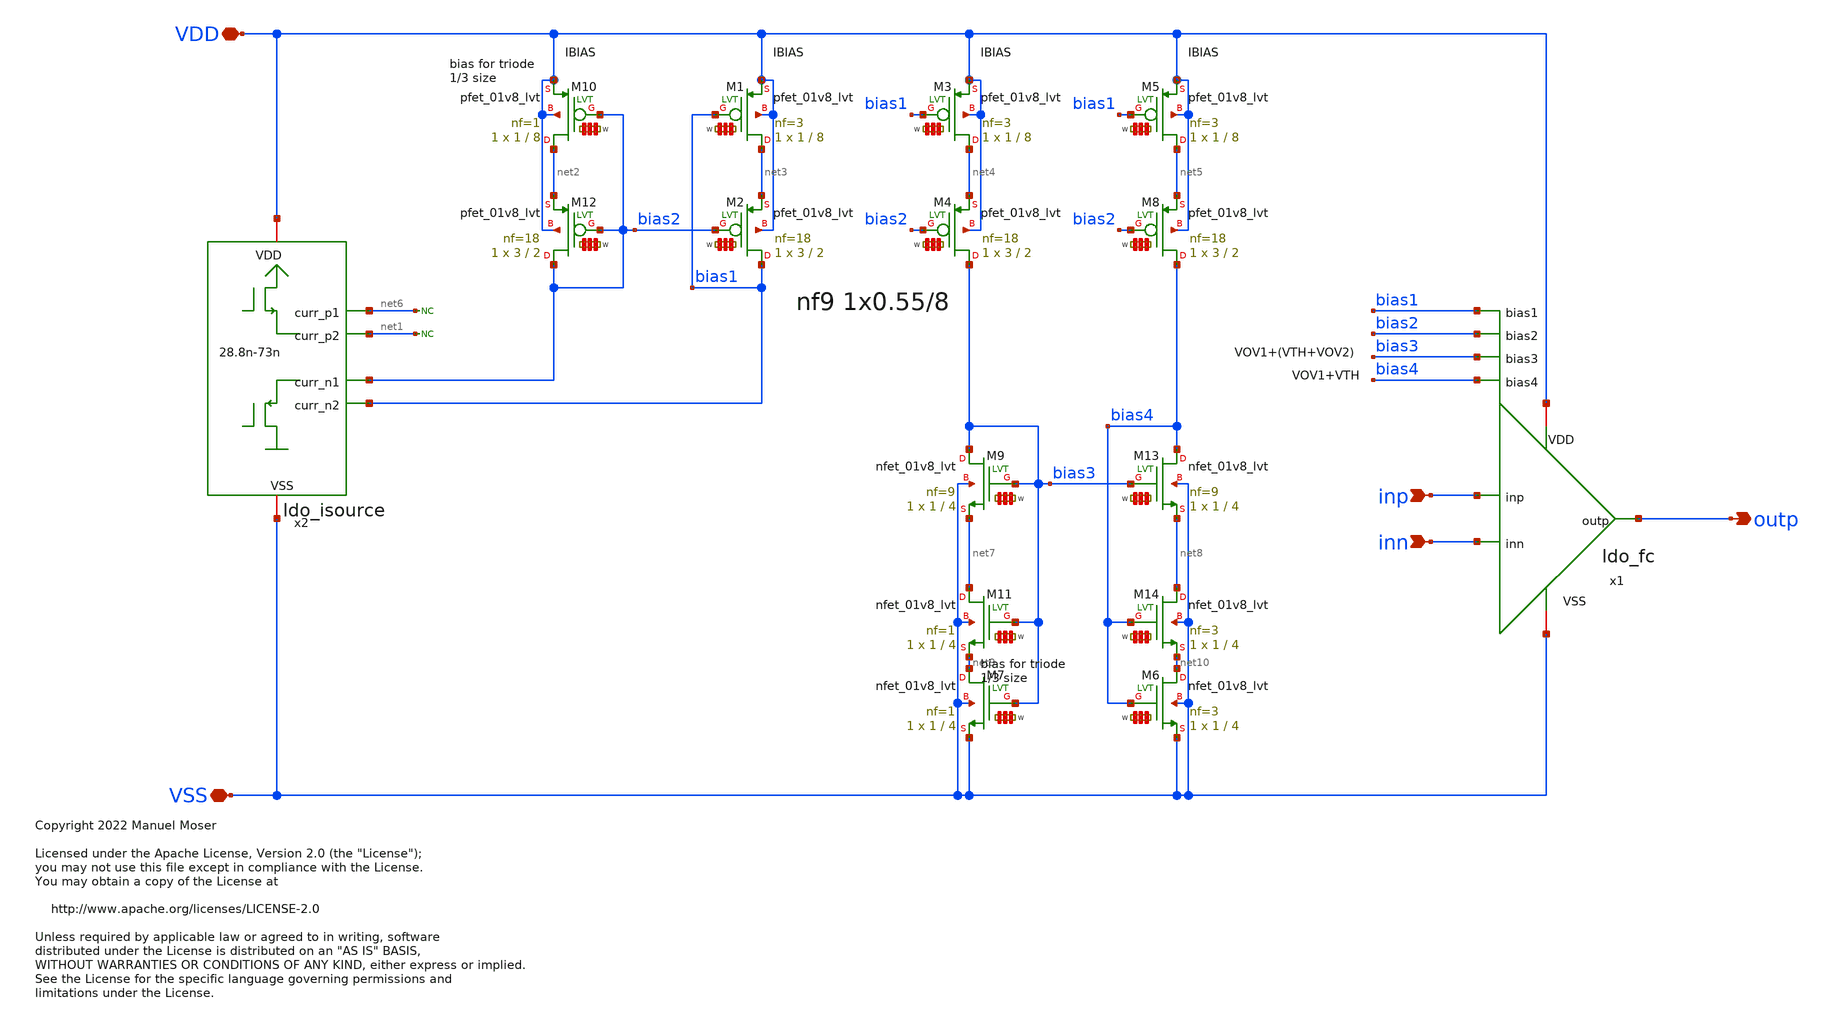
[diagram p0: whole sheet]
** sch_path: xschem/ldo_ota.sch
* Copyright 2022 Manuel Moser
* Licensed under the Apache License, Version 2.0 (the "License");
**.subckt ldo_ota VDD VSS inp inn outp
*.iopin VDD
*.iopin VSS
*.ipin inp
*.ipin inn
*.opin outp
x1 VDD inp inn bias1 bias2 bias3 outp VSS bias4 ldo_fc
x2 net1 bias2 VDD VSS bias1 net6 ldo_isource
XM10 net2 bias2 VDD VDD sky130_fd_pr__pfet_01v8_lvt L=8 W='1 * 1 ' nf=1 ad='int((nf+1)/2) * W / nf * 0.29'
+ as='int((nf+2)/2) * W / nf * 0.29' pd='2*int((nf+1)/2) * (W / nf + 0.29)' ps='2*int((nf+2)/2) * (W / nf + 0.29)'
+ nrd='0.29 / W ' nrs='0.29 / W ' sa=0 sb=0 sd=0 mult=1 m=1
XM12 bias2 bias2 net2 VDD sky130_fd_pr__pfet_01v8_lvt L=2 W='3 * 18 ' nf=18 ad='int((nf+1)/2) * W / nf * 0.29'
+ as='int((nf+2)/2) * W / nf * 0.29' pd='2*int((nf+1)/2) * (W / nf + 0.29)' ps='2*int((nf+2)/2) * (W / nf + 0.29)'
+ nrd='0.29 / W ' nrs='0.29 / W ' sa=0 sb=0 sd=0 mult=1 m=1
* noconn #net1
XM1 net3 bias1 VDD VDD sky130_fd_pr__pfet_01v8_lvt L=8 W='1 * 3 ' nf=3 ad='int((nf+1)/2) * W / nf * 0.29'
+ as='int((nf+2)/2) * W / nf * 0.29' pd='2*int((nf+1)/2) * (W / nf + 0.29)' ps='2*int((nf+2)/2) * (W / nf + 0.29)'
+ nrd='0.29 / W ' nrs='0.29 / W ' sa=0 sb=0 sd=0 mult=1 m=1
XM2 bias1 bias2 net3 VDD sky130_fd_pr__pfet_01v8_lvt L=2 W='3 * 18 ' nf=18 ad='int((nf+1)/2) * W / nf * 0.29'
+ as='int((nf+2)/2) * W / nf * 0.29' pd='2*int((nf+1)/2) * (W / nf + 0.29)' ps='2*int((nf+2)/2) * (W / nf + 0.29)'
+ nrd='0.29 / W ' nrs='0.29 / W ' sa=0 sb=0 sd=0 mult=1 m=1
XM3 net4 bias1 VDD VDD sky130_fd_pr__pfet_01v8_lvt L=8 W='1 * 3 ' nf=3 ad='int((nf+1)/2) * W / nf * 0.29'
+ as='int((nf+2)/2) * W / nf * 0.29' pd='2*int((nf+1)/2) * (W / nf + 0.29)' ps='2*int((nf+2)/2) * (W / nf + 0.29)'
+ nrd='0.29 / W ' nrs='0.29 / W ' sa=0 sb=0 sd=0 mult=1 m=1
XM4 bias3 bias2 net4 VDD sky130_fd_pr__pfet_01v8_lvt L=2 W='3 * 18 ' nf=18 ad='int((nf+1)/2) * W / nf * 0.29'
+ as='int((nf+2)/2) * W / nf * 0.29' pd='2*int((nf+1)/2) * (W / nf + 0.29)' ps='2*int((nf+2)/2) * (W / nf + 0.29)'
+ nrd='0.29 / W ' nrs='0.29 / W ' sa=0 sb=0 sd=0 mult=1 m=1
XM5 net5 bias1 VDD VDD sky130_fd_pr__pfet_01v8_lvt L=8 W='1 * 3 ' nf=3 ad='int((nf+1)/2) * W / nf * 0.29'
+ as='int((nf+2)/2) * W / nf * 0.29' pd='2*int((nf+1)/2) * (W / nf + 0.29)' ps='2*int((nf+2)/2) * (W / nf + 0.29)'
+ nrd='0.29 / W ' nrs='0.29 / W ' sa=0 sb=0 sd=0 mult=1 m=1
XM8 bias4 bias2 net5 VDD sky130_fd_pr__pfet_01v8_lvt L=2 W='3 * 18 ' nf=18 ad='int((nf+1)/2) * W / nf * 0.29'
+ as='int((nf+2)/2) * W / nf * 0.29' pd='2*int((nf+1)/2) * (W / nf + 0.29)' ps='2*int((nf+2)/2) * (W / nf + 0.29)'
+ nrd='0.29 / W ' nrs='0.29 / W ' sa=0 sb=0 sd=0 mult=1 m=1
* noconn #net6
XM9 bias3 bias3 net7 VSS sky130_fd_pr__nfet_01v8_lvt L=4 W='1 * 9 ' nf=9 ad='int((nf+1)/2) * W / nf * 0.29'
+ as='int((nf+2)/2) * W / nf * 0.29' pd='2*int((nf+1)/2) * (W / nf + 0.29)' ps='2*int((nf+2)/2) * (W / nf + 0.29)'
+ nrd='0.29 / W ' nrs='0.29 / W ' sa=0 sb=0 sd=0 mult=1 m=1
XM11 net7 bias3 net9 VSS sky130_fd_pr__nfet_01v8_lvt L=4 W='1 * 1 ' nf=1 ad='int((nf+1)/2) * W / nf * 0.29'
+ as='int((nf+2)/2) * W / nf * 0.29' pd='2*int((nf+1)/2) * (W / nf + 0.29)' ps='2*int((nf+2)/2) * (W / nf + 0.29)'
+ nrd='0.29 / W ' nrs='0.29 / W ' sa=0 sb=0 sd=0 mult=1 m=1
XM13 bias4 bias3 net8 VSS sky130_fd_pr__nfet_01v8_lvt L=4 W='1 * 9 ' nf=9 ad='int((nf+1)/2) * W / nf * 0.29'
+ as='int((nf+2)/2) * W / nf * 0.29' pd='2*int((nf+1)/2) * (W / nf + 0.29)' ps='2*int((nf+2)/2) * (W / nf + 0.29)'
+ nrd='0.29 / W ' nrs='0.29 / W ' sa=0 sb=0 sd=0 mult=1 m=1
XM14 net8 bias4 net10 VSS sky130_fd_pr__nfet_01v8_lvt L=4 W='1 * 3 ' nf=3 ad='int((nf+1)/2) * W / nf * 0.29'
+ as='int((nf+2)/2) * W / nf * 0.29' pd='2*int((nf+1)/2) * (W / nf + 0.29)' ps='2*int((nf+2)/2) * (W / nf + 0.29)'
+ nrd='0.29 / W ' nrs='0.29 / W ' sa=0 sb=0 sd=0 mult=1 m=1
XM6 net10 bias4 VSS VSS sky130_fd_pr__nfet_01v8_lvt L=4 W='1 * 3 ' nf=3 ad='int((nf+1)/2) * W / nf * 0.29'
+ as='int((nf+2)/2) * W / nf * 0.29' pd='2*int((nf+1)/2) * (W / nf + 0.29)' ps='2*int((nf+2)/2) * (W / nf + 0.29)'
+ nrd='0.29 / W ' nrs='0.29 / W ' sa=0 sb=0 sd=0 mult=1 m=1
XM7 net9 bias3 VSS VSS sky130_fd_pr__nfet_01v8_lvt L=4 W='1 * 1 ' nf=1 ad='int((nf+1)/2) * W / nf * 0.29'
+ as='int((nf+2)/2) * W / nf * 0.29' pd='2*int((nf+1)/2) * (W / nf + 0.29)' ps='2*int((nf+2)/2) * (W / nf + 0.29)'
+ nrd='0.29 / W ' nrs='0.29 / W ' sa=0 sb=0 sd=0 mult=1 m=1
**.ends

* expanding   symbol:  ldo_fc.sym # of pins=9
** sym_path: xschem/ldo_fc.sym
** sch_path: xschem/ldo_fc.sch
.subckt ldo_fc VDD inp inn bias1 bias2 bias3 outp VSS bias4
*.iopin VSS
*.iopin VDD
*.ipin inp
*.ipin inn
*.ipin bias1
*.opin outp
*.ipin bias2
*.ipin bias3
*.ipin bias4
XMN4 outp bias3 net1 VSS sky130_fd_pr__nfet_01v8_lvt L=4 W='1 * 9 ' nf=9 ad='int((nf+1)/2) * W / nf * 0.29'
+ as='int((nf+2)/2) * W / nf * 0.29' pd='2*int((nf+1)/2) * (W / nf + 0.29)' ps='2*int((nf+2)/2) * (W / nf + 0.29)'
+ nrd='0.29 / W ' nrs='0.29 / W ' sa=0 sb=0 sd=0 mult=12 m=12
XMN7 net1 net3 net8 VSS sky130_fd_pr__nfet_01v8_lvt L=4 W='1 * 3 ' nf=3 ad='int((nf+1)/2) * W / nf * 0.29'
+ as='int((nf+2)/2) * W / nf * 0.29' pd='2*int((nf+1)/2) * (W / nf + 0.29)' ps='2*int((nf+2)/2) * (W / nf + 0.29)'
+ nrd='0.29 / W ' nrs='0.29 / W ' sa=0 sb=0 sd=0 mult=12 m=12
XMN3 net3 bias3 net2 VSS sky130_fd_pr__nfet_01v8_lvt L=4 W='1 * 9 ' nf=9 ad='int((nf+1)/2) * W / nf * 0.29'
+ as='int((nf+2)/2) * W / nf * 0.29' pd='2*int((nf+1)/2) * (W / nf + 0.29)' ps='2*int((nf+2)/2) * (W / nf + 0.29)'
+ nrd='0.29 / W ' nrs='0.29 / W ' sa=0 sb=0 sd=0 mult=12 m=12
XMN6 net2 net3 net7 VSS sky130_fd_pr__nfet_01v8_lvt L=4 W='1 * 3 ' nf=3 ad='int((nf+1)/2) * W / nf * 0.29'
+ as='int((nf+2)/2) * W / nf * 0.29' pd='2*int((nf+1)/2) * (W / nf + 0.29)' ps='2*int((nf+2)/2) * (W / nf + 0.29)'
+ nrd='0.29 / W ' nrs='0.29 / W ' sa=0 sb=0 sd=0 mult=12 m=12
XMP4 outp bias2 net5 VDD sky130_fd_pr__pfet_01v8_lvt L=2 W='3 * 18 ' nf=18 ad='int((nf+1)/2) * W / nf * 0.29'
+ as='int((nf+2)/2) * W / nf * 0.29' pd='2*int((nf+1)/2) * (W / nf + 0.29)' ps='2*int((nf+2)/2) * (W / nf + 0.29)'
+ nrd='0.29 / W ' nrs='0.29 / W ' sa=0 sb=0 sd=0 mult=12 m=12
XMP2 net5 bias1 VDD VDD sky130_fd_pr__pfet_01v8_lvt L=8 W='1 * 3 ' nf=3 ad='int((nf+1)/2) * W / nf * 0.29'
+ as='int((nf+2)/2) * W / nf * 0.29' pd='2*int((nf+1)/2) * (W / nf + 0.29)' ps='2*int((nf+2)/2) * (W / nf + 0.29)'
+ nrd='0.29 / W ' nrs='0.29 / W ' sa=0 sb=0 sd=0 mult=19 m=19
XMP3 net3 bias2 net4 VDD sky130_fd_pr__pfet_01v8_lvt L=2 W='3 * 18 ' nf=18 ad='int((nf+1)/2) * W / nf * 0.29'
+ as='int((nf+2)/2) * W / nf * 0.29' pd='2*int((nf+1)/2) * (W / nf + 0.29)' ps='2*int((nf+2)/2) * (W / nf + 0.29)'
+ nrd='0.29 / W ' nrs='0.29 / W ' sa=0 sb=0 sd=0 mult=12 m=12
XMP1 net4 bias1 VDD VDD sky130_fd_pr__pfet_01v8_lvt L=8 W='1 * 3 ' nf=3 ad='int((nf+1)/2) * W / nf * 0.29'
+ as='int((nf+2)/2) * W / nf * 0.29' pd='2*int((nf+1)/2) * (W / nf + 0.29)' ps='2*int((nf+2)/2) * (W / nf + 0.29)'
+ nrd='0.29 / W ' nrs='0.29 / W ' sa=0 sb=0 sd=0 mult=19 m=19
XMN5 net6 bias4 net9 VSS sky130_fd_pr__nfet_01v8_lvt L=4 W='1 * 3 ' nf=3 ad='int((nf+1)/2) * W / nf * 0.29'
+ as='int((nf+2)/2) * W / nf * 0.29' pd='2*int((nf+1)/2) * (W / nf + 0.29)' ps='2*int((nf+2)/2) * (W / nf + 0.29)'
+ nrd='0.29 / W ' nrs='0.29 / W ' sa=0 sb=0 sd=0 mult=14 m=14
XMN1 net4 inp net6 VSS sky130_fd_pr__nfet_01v8_lvt L=0.25 W='7 * 5 ' nf=5 ad='int((nf+1)/2) * W / nf * 0.29'
+ as='int((nf+2)/2) * W / nf * 0.29' pd='2*int((nf+1)/2) * (W / nf + 0.29)' ps='2*int((nf+2)/2) * (W / nf + 0.29)'
+ nrd='0.29 / W ' nrs='0.29 / W ' sa=0 sb=0 sd=0 mult=1 m=1
XMN2 net5 inn net6 VSS sky130_fd_pr__nfet_01v8_lvt L=0.25 W='7 * 5 ' nf=5 ad='int((nf+1)/2) * W / nf * 0.29'
+ as='int((nf+2)/2) * W / nf * 0.29' pd='2*int((nf+1)/2) * (W / nf + 0.29)' ps='2*int((nf+2)/2) * (W / nf + 0.29)'
+ nrd='0.29 / W ' nrs='0.29 / W ' sa=0 sb=0 sd=0 mult=1 m=1
XMN9 net8 net3 VSS VSS sky130_fd_pr__nfet_01v8_lvt L=4 W='1 * 3 ' nf=3 ad='int((nf+1)/2) * W / nf * 0.29'
+ as='int((nf+2)/2) * W / nf * 0.29' pd='2*int((nf+1)/2) * (W / nf + 0.29)' ps='2*int((nf+2)/2) * (W / nf + 0.29)'
+ nrd='0.29 / W ' nrs='0.29 / W ' sa=0 sb=0 sd=0 mult=12 m=12
XMN10 net7 net3 VSS VSS sky130_fd_pr__nfet_01v8_lvt L=4 W='1 * 3 ' nf=3 ad='int((nf+1)/2) * W / nf * 0.29'
+ as='int((nf+2)/2) * W / nf * 0.29' pd='2*int((nf+1)/2) * (W / nf + 0.29)' ps='2*int((nf+2)/2) * (W / nf + 0.29)'
+ nrd='0.29 / W ' nrs='0.29 / W ' sa=0 sb=0 sd=0 mult=12 m=12
XMN11 net9 bias4 VSS VSS sky130_fd_pr__nfet_01v8_lvt L=4 W='1 * 3 ' nf=3 ad='int((nf+1)/2) * W / nf * 0.29'
+ as='int((nf+2)/2) * W / nf * 0.29' pd='2*int((nf+1)/2) * (W / nf + 0.29)' ps='2*int((nf+2)/2) * (W / nf + 0.29)'
+ nrd='0.29 / W ' nrs='0.29 / W ' sa=0 sb=0 sd=0 mult=14 m=14
.ends


* expanding   symbol:  ldo_isource.sym # of pins=6
** sym_path: xschem/ldo_isource.sym
** sch_path: xschem/ldo_isource.sch
.subckt ldo_isource curr_p2 curr_n1 VDD VSS curr_n2 curr_p1
*.iopin VDD
*.iopin VSS
*.ipin curr_n1
*.opin curr_p1
*.ipin curr_n2
*.opin curr_p2
XMP2 VGP VGP net4 VDD sky130_fd_pr__pfet_01v8_lvt L=8 W='0.55 * 7 ' nf=7 ad='int((nf+1)/2) * W / nf * 0.29'
+ as='int((nf+2)/2) * W / nf * 0.29' pd='2*int((nf+1)/2) * (W / nf + 0.29)' ps='2*int((nf+2)/2) * (W / nf + 0.29)'
+ nrd='0.29 / W ' nrs='0.29 / W ' sa=0 sb=0 sd=0 mult=1 m=1
XMP1 VGN VGP net3 VDD sky130_fd_pr__pfet_01v8_lvt L=8 W='0.55 * 7 ' nf=7 ad='int((nf+1)/2) * W / nf * 0.29'
+ as='int((nf+2)/2) * W / nf * 0.29' pd='2*int((nf+1)/2) * (W / nf + 0.29)' ps='2*int((nf+2)/2) * (W / nf + 0.29)'
+ nrd='0.29 / W ' nrs='0.29 / W ' sa=0 sb=0 sd=0 mult=1 m=1
XMN1 VGN VGN net1 VSS sky130_fd_pr__nfet_01v8_lvt L=8 W='7 * 1 ' nf=1 ad='int((nf+1)/2) * W / nf * 0.29'
+ as='int((nf+2)/2) * W / nf * 0.29' pd='2*int((nf+1)/2) * (W / nf + 0.29)' ps='2*int((nf+2)/2) * (W / nf + 0.29)'
+ nrd='0.29 / W ' nrs='0.29 / W ' sa=0 sb=0 sd=0 mult=1 m=1
XMN2 VGP VGN net2 VSS sky130_fd_pr__nfet_01v8_lvt L=8 W='7 * 1 ' nf=1 ad='int((nf+1)/2) * W / nf * 0.29'
+ as='int((nf+2)/2) * W / nf * 0.29' pd='2*int((nf+1)/2) * (W / nf + 0.29)' ps='2*int((nf+2)/2) * (W / nf + 0.29)'
+ nrd='0.29 / W ' nrs='0.29 / W ' sa=0 sb=0 sd=0 mult=5 m=5
XMN3 net1 VGN VSS VSS sky130_fd_pr__nfet_01v8_lvt L=8 W='7 * 1 ' nf=1 ad='int((nf+1)/2) * W / nf * 0.29'
+ as='int((nf+2)/2) * W / nf * 0.29' pd='2*int((nf+1)/2) * (W / nf + 0.29)' ps='2*int((nf+2)/2) * (W / nf + 0.29)'
+ nrd='0.29 / W ' nrs='0.29 / W ' sa=0 sb=0 sd=0 mult=1 m=1
XMN4 net2 VGN Vref VSS sky130_fd_pr__nfet_01v8_lvt L=8 W='7 * 1 ' nf=1 ad='int((nf+1)/2) * W / nf * 0.29'
+ as='int((nf+2)/2) * W / nf * 0.29' pd='2*int((nf+1)/2) * (W / nf + 0.29)' ps='2*int((nf+2)/2) * (W / nf + 0.29)'
+ nrd='0.29 / W ' nrs='0.29 / W ' sa=0 sb=0 sd=0 mult=5 m=5
XMP4 net3 VGP VDD VDD sky130_fd_pr__pfet_01v8_lvt L=8 W='0.55 * 7 ' nf=7 ad='int((nf+1)/2) * W / nf * 0.29'
+ as='int((nf+2)/2) * W / nf * 0.29' pd='2*int((nf+1)/2) * (W / nf + 0.29)' ps='2*int((nf+2)/2) * (W / nf + 0.29)'
+ nrd='0.29 / W ' nrs='0.29 / W ' sa=0 sb=0 sd=0 mult=1 m=1
XMP5 net4 VGP VDD VDD sky130_fd_pr__pfet_01v8_lvt L=8 W='0.55 * 7 ' nf=7 ad='int((nf+1)/2) * W / nf * 0.29'
+ as='int((nf+2)/2) * W / nf * 0.29' pd='2*int((nf+1)/2) * (W / nf + 0.29)' ps='2*int((nf+2)/2) * (W / nf + 0.29)'
+ nrd='0.29 / W ' nrs='0.29 / W ' sa=0 sb=0 sd=0 mult=1 m=1
XMP3 Vrefgate VGP net19 VDD sky130_fd_pr__pfet_01v8_lvt L=8 W='0.55 * 7 ' nf=7 ad='int((nf+1)/2) * W / nf * 0.29'
+ as='int((nf+2)/2) * W / nf * 0.29' pd='2*int((nf+1)/2) * (W / nf + 0.29)' ps='2*int((nf+2)/2) * (W / nf + 0.29)'
+ nrd='0.29 / W ' nrs='0.29 / W ' sa=0 sb=0 sd=0 mult=1 m=1
XM2 net5 Vrefgate net6 VSS sky130_fd_pr__nfet_01v8 L=4 W='1 * 1 ' nf=1 ad='int((nf+1)/2) * W / nf * 0.29'
+ as='int((nf+2)/2) * W / nf * 0.29' pd='2*int((nf+1)/2) * (W / nf + 0.29)' ps='2*int((nf+2)/2) * (W / nf + 0.29)'
+ nrd='0.29 / W ' nrs='0.29 / W ' sa=0 sb=0 sd=0 mult=1 m=1
XM3 net8 Vrefgate VSS VSS sky130_fd_pr__nfet_01v8 L=4 W='1 * 1 ' nf=1 ad='int((nf+1)/2) * W / nf * 0.29'
+ as='int((nf+2)/2) * W / nf * 0.29' pd='2*int((nf+1)/2) * (W / nf + 0.29)' ps='2*int((nf+2)/2) * (W / nf + 0.29)'
+ nrd='0.29 / W ' nrs='0.29 / W ' sa=0 sb=0 sd=0 mult=1 m=1
XM1 net7 Vrefgate net8 VSS sky130_fd_pr__nfet_01v8 L=4 W='1 * 1 ' nf=1 ad='int((nf+1)/2) * W / nf * 0.29'
+ as='int((nf+2)/2) * W / nf * 0.29' pd='2*int((nf+1)/2) * (W / nf + 0.29)' ps='2*int((nf+2)/2) * (W / nf + 0.29)'
+ nrd='0.29 / W ' nrs='0.29 / W ' sa=0 sb=0 sd=0 mult=1 m=1
XM4 net6 Vrefgate net7 VSS sky130_fd_pr__nfet_01v8 L=4 W='1 * 1 ' nf=1 ad='int((nf+1)/2) * W / nf * 0.29'
+ as='int((nf+2)/2) * W / nf * 0.29' pd='2*int((nf+1)/2) * (W / nf + 0.29)' ps='2*int((nf+2)/2) * (W / nf + 0.29)'
+ nrd='0.29 / W ' nrs='0.29 / W ' sa=0 sb=0 sd=0 mult=1 m=1
XMN5 net10 Vrefgate VSS VSS sky130_fd_pr__nfet_01v8_lvt L=4 W='1 * 1 ' nf=1 ad='int((nf+1)/2) * W / nf * 0.29'
+ as='int((nf+2)/2) * W / nf * 0.29' pd='2*int((nf+1)/2) * (W / nf + 0.29)' ps='2*int((nf+2)/2) * (W / nf + 0.29)'
+ nrd='0.29 / W ' nrs='0.29 / W ' sa=0 sb=0 sd=0 mult=1 m=1
XMN6 net14 Vrefgate net9 VSS sky130_fd_pr__nfet_01v8_lvt L=4 W='1 * 1 ' nf=1 ad='int((nf+1)/2) * W / nf * 0.29'
+ as='int((nf+2)/2) * W / nf * 0.29' pd='2*int((nf+1)/2) * (W / nf + 0.29)' ps='2*int((nf+2)/2) * (W / nf + 0.29)'
+ nrd='0.29 / W ' nrs='0.29 / W ' sa=0 sb=0 sd=0 mult=1 m=1
XMN9 net16 Vrefgate net14 VSS sky130_fd_pr__nfet_01v8_lvt L=4 W='1 * 1 ' nf=1 ad='int((nf+1)/2) * W / nf * 0.29'
+ as='int((nf+2)/2) * W / nf * 0.29' pd='2*int((nf+1)/2) * (W / nf + 0.29)' ps='2*int((nf+2)/2) * (W / nf + 0.29)'
+ nrd='0.29 / W ' nrs='0.29 / W ' sa=0 sb=0 sd=0 mult=1 m=1
XM5 Vrefgate Vrefgate net5 VSS sky130_fd_pr__nfet_01v8 L=4 W='1 * 1 ' nf=1 ad='int((nf+1)/2) * W / nf * 0.29'
+ as='int((nf+2)/2) * W / nf * 0.29' pd='2*int((nf+1)/2) * (W / nf + 0.29)' ps='2*int((nf+2)/2) * (W / nf + 0.29)'
+ nrd='0.29 / W ' nrs='0.29 / W ' sa=0 sb=0 sd=0 mult=1 m=1
XMN10 net11 Vrefgate net10 VSS sky130_fd_pr__nfet_01v8_lvt L=4 W='1 * 1 ' nf=1 ad='int((nf+1)/2) * W / nf * 0.29'
+ as='int((nf+2)/2) * W / nf * 0.29' pd='2*int((nf+1)/2) * (W / nf + 0.29)' ps='2*int((nf+2)/2) * (W / nf + 0.29)'
+ nrd='0.29 / W ' nrs='0.29 / W ' sa=0 sb=0 sd=0 mult=1 m=1
XMN11 net12 Vrefgate net11 VSS sky130_fd_pr__nfet_01v8_lvt L=4 W='1 * 1 ' nf=1 ad='int((nf+1)/2) * W / nf * 0.29'
+ as='int((nf+2)/2) * W / nf * 0.29' pd='2*int((nf+1)/2) * (W / nf + 0.29)' ps='2*int((nf+2)/2) * (W / nf + 0.29)'
+ nrd='0.29 / W ' nrs='0.29 / W ' sa=0 sb=0 sd=0 mult=1 m=1
XMN12 net13 Vrefgate net12 VSS sky130_fd_pr__nfet_01v8_lvt L=4 W='1 * 1 ' nf=1 ad='int((nf+1)/2) * W / nf * 0.29'
+ as='int((nf+2)/2) * W / nf * 0.29' pd='2*int((nf+1)/2) * (W / nf + 0.29)' ps='2*int((nf+2)/2) * (W / nf + 0.29)'
+ nrd='0.29 / W ' nrs='0.29 / W ' sa=0 sb=0 sd=0 mult=1 m=1
XMN13 net9 Vrefgate net13 VSS sky130_fd_pr__nfet_01v8_lvt L=4 W='1 * 1 ' nf=1 ad='int((nf+1)/2) * W / nf * 0.29'
+ as='int((nf+2)/2) * W / nf * 0.29' pd='2*int((nf+1)/2) * (W / nf + 0.29)' ps='2*int((nf+2)/2) * (W / nf + 0.29)'
+ nrd='0.29 / W ' nrs='0.29 / W ' sa=0 sb=0 sd=0 mult=1 m=1
XMN7 net18 Vrefgate net15 VSS sky130_fd_pr__nfet_01v8_lvt L=4 W='1 * 1 ' nf=1 ad='int((nf+1)/2) * W / nf * 0.29'
+ as='int((nf+2)/2) * W / nf * 0.29' pd='2*int((nf+1)/2) * (W / nf + 0.29)' ps='2*int((nf+2)/2) * (W / nf + 0.29)'
+ nrd='0.29 / W ' nrs='0.29 / W ' sa=0 sb=0 sd=0 mult=1 m=1
XMN8 Vref Vrefgate net18 VSS sky130_fd_pr__nfet_01v8_lvt L=4 W='1 * 1 ' nf=1 ad='int((nf+1)/2) * W / nf * 0.29'
+ as='int((nf+2)/2) * W / nf * 0.29' pd='2*int((nf+1)/2) * (W / nf + 0.29)' ps='2*int((nf+2)/2) * (W / nf + 0.29)'
+ nrd='0.29 / W ' nrs='0.29 / W ' sa=0 sb=0 sd=0 mult=1 m=1
XMN14 net17 Vrefgate net16 VSS sky130_fd_pr__nfet_01v8_lvt L=4 W='1 * 1 ' nf=1 ad='int((nf+1)/2) * W / nf * 0.29'
+ as='int((nf+2)/2) * W / nf * 0.29' pd='2*int((nf+1)/2) * (W / nf + 0.29)' ps='2*int((nf+2)/2) * (W / nf + 0.29)'
+ nrd='0.29 / W ' nrs='0.29 / W ' sa=0 sb=0 sd=0 mult=1 m=1
XMN15 net15 Vrefgate net17 VSS sky130_fd_pr__nfet_01v8_lvt L=4 W='1 * 1 ' nf=1 ad='int((nf+1)/2) * W / nf * 0.29'
+ as='int((nf+2)/2) * W / nf * 0.29' pd='2*int((nf+1)/2) * (W / nf + 0.29)' ps='2*int((nf+2)/2) * (W / nf + 0.29)'
+ nrd='0.29 / W ' nrs='0.29 / W ' sa=0 sb=0 sd=0 mult=1 m=1
XMP6 net19 VGP VDD VDD sky130_fd_pr__pfet_01v8_lvt L=8 W='0.55 * 7 ' nf=7 ad='int((nf+1)/2) * W / nf * 0.29'
+ as='int((nf+2)/2) * W / nf * 0.29' pd='2*int((nf+1)/2) * (W / nf + 0.29)' ps='2*int((nf+2)/2) * (W / nf + 0.29)'
+ nrd='0.29 / W ' nrs='0.29 / W ' sa=0 sb=0 sd=0 mult=1 m=1
XMP7 curr_p1 VGP net20 VDD sky130_fd_pr__pfet_01v8_lvt L=8 W='0.55 * 7 ' nf=7 ad='int((nf+1)/2) * W / nf * 0.29'
+ as='int((nf+2)/2) * W / nf * 0.29' pd='2*int((nf+1)/2) * (W / nf + 0.29)' ps='2*int((nf+2)/2) * (W / nf + 0.29)'
+ nrd='0.29 / W ' nrs='0.29 / W ' sa=0 sb=0 sd=0 mult=1 m=1
XMP8 net20 VGP VDD VDD sky130_fd_pr__pfet_01v8_lvt L=8 W='0.55 * 7 ' nf=7 ad='int((nf+1)/2) * W / nf * 0.29'
+ as='int((nf+2)/2) * W / nf * 0.29' pd='2*int((nf+1)/2) * (W / nf + 0.29)' ps='2*int((nf+2)/2) * (W / nf + 0.29)'
+ nrd='0.29 / W ' nrs='0.29 / W ' sa=0 sb=0 sd=0 mult=1 m=1
XMN16 curr_n1 VGN net21 VSS sky130_fd_pr__nfet_01v8_lvt L=8 W='7 * 1 ' nf=1 ad='int((nf+1)/2) * W / nf * 0.29'
+ as='int((nf+2)/2) * W / nf * 0.29' pd='2*int((nf+1)/2) * (W / nf + 0.29)' ps='2*int((nf+2)/2) * (W / nf + 0.29)'
+ nrd='0.29 / W ' nrs='0.29 / W ' sa=0 sb=0 sd=0 mult=1 m=1
XMN17 net21 VGN VSS VSS sky130_fd_pr__nfet_01v8_lvt L=8 W='7 * 1 ' nf=1 ad='int((nf+1)/2) * W / nf * 0.29'
+ as='int((nf+2)/2) * W / nf * 0.29' pd='2*int((nf+1)/2) * (W / nf + 0.29)' ps='2*int((nf+2)/2) * (W / nf + 0.29)'
+ nrd='0.29 / W ' nrs='0.29 / W ' sa=0 sb=0 sd=0 mult=1 m=1
XM6 VGP net22 VGN VSS sky130_fd_pr__nfet_01v8 L=4 W='1 * 1 ' nf=1 ad='int((nf+1)/2) * W / nf * 0.29'
+ as='int((nf+2)/2) * W / nf * 0.29' pd='2*int((nf+1)/2) * (W / nf + 0.29)' ps='2*int((nf+2)/2) * (W / nf + 0.29)'
+ nrd='0.29 / W ' nrs='0.29 / W ' sa=0 sb=0 sd=0 mult=1 m=1
XM7 net22 Vrefgate VSS VSS sky130_fd_pr__nfet_01v8 L=4 W='1 * 1 ' nf=1 ad='int((nf+1)/2) * W / nf * 0.29'
+ as='int((nf+2)/2) * W / nf * 0.29' pd='2*int((nf+1)/2) * (W / nf + 0.29)' ps='2*int((nf+2)/2) * (W / nf + 0.29)'
+ nrd='0.29 / W ' nrs='0.29 / W ' sa=0 sb=0 sd=0 mult=1 m=1
XC1 VDD net22 VSS sky130_fd_pr__cap_var_hvt W=2 L=2 VM=1 m=1
XMP9 curr_p2 VGP net23 VDD sky130_fd_pr__pfet_01v8_lvt L=8 W='0.55 * 7 ' nf=7 ad='int((nf+1)/2) * W / nf * 0.29'
+ as='int((nf+2)/2) * W / nf * 0.29' pd='2*int((nf+1)/2) * (W / nf + 0.29)' ps='2*int((nf+2)/2) * (W / nf + 0.29)'
+ nrd='0.29 / W ' nrs='0.29 / W ' sa=0 sb=0 sd=0 mult=1 m=1
XMP10 net23 VGP VDD VDD sky130_fd_pr__pfet_01v8_lvt L=8 W='0.55 * 7 ' nf=7 ad='int((nf+1)/2) * W / nf * 0.29'
+ as='int((nf+2)/2) * W / nf * 0.29' pd='2*int((nf+1)/2) * (W / nf + 0.29)' ps='2*int((nf+2)/2) * (W / nf + 0.29)'
+ nrd='0.29 / W ' nrs='0.29 / W ' sa=0 sb=0 sd=0 mult=1 m=1
XMN18 curr_n2 VGN net24 VSS sky130_fd_pr__nfet_01v8_lvt L=8 W='7 * 1 ' nf=1 ad='int((nf+1)/2) * W / nf * 0.29'
+ as='int((nf+2)/2) * W / nf * 0.29' pd='2*int((nf+1)/2) * (W / nf + 0.29)' ps='2*int((nf+2)/2) * (W / nf + 0.29)'
+ nrd='0.29 / W ' nrs='0.29 / W ' sa=0 sb=0 sd=0 mult=1 m=1
XMN19 net24 VGN VSS VSS sky130_fd_pr__nfet_01v8_lvt L=8 W='7 * 1 ' nf=1 ad='int((nf+1)/2) * W / nf * 0.29'
+ as='int((nf+2)/2) * W / nf * 0.29' pd='2*int((nf+1)/2) * (W / nf + 0.29)' ps='2*int((nf+2)/2) * (W / nf + 0.29)'
+ nrd='0.29 / W ' nrs='0.29 / W ' sa=0 sb=0 sd=0 mult=1 m=1
.ends

.end
